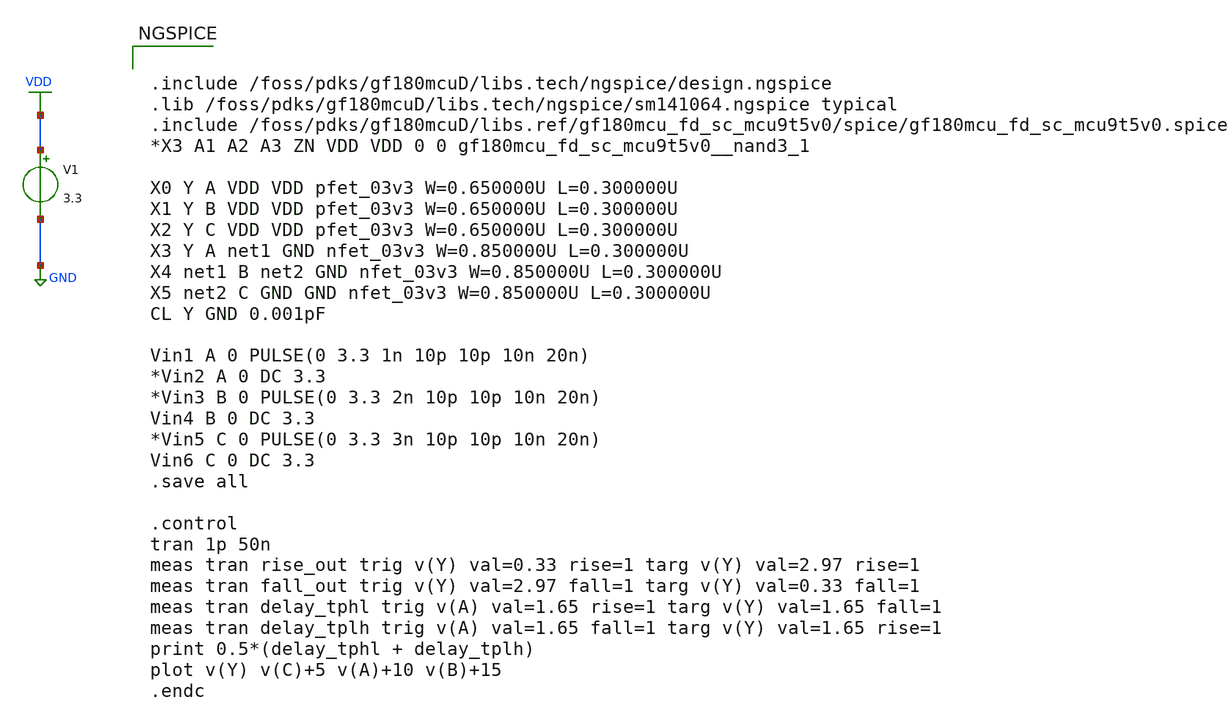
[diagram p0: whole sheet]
** sch_path: designs/libs/tb_NAND3/nand3_test.sch
**.subckt nand3_test
V1 VDD GND 3.3
**** begin user architecture code


.include /foss/pdks/gf180mcuD/libs.tech/ngspice/design.ngspice
.lib /foss/pdks/gf180mcuD/libs.tech/ngspice/sm141064.ngspice typical
.include /foss/pdks/gf180mcuD/libs.ref/gf180mcu_fd_sc_mcu9t5v0/spice/gf180mcu_fd_sc_mcu9t5v0.spice
*X3 A1 A2 A3 ZN VDD VDD 0 0 gf180mcu_fd_sc_mcu9t5v0__nand3_1

X0 Y A VDD VDD pfet_03v3 W=0.650000U L=0.300000U
X1 Y B VDD VDD pfet_03v3 W=0.650000U L=0.300000U
X2 Y C VDD VDD pfet_03v3 W=0.650000U L=0.300000U
X3 Y A net1 GND nfet_03v3 W=0.850000U L=0.300000U
X4 net1 B net2 GND nfet_03v3 W=0.850000U L=0.300000U
X5 net2 C GND GND nfet_03v3 W=0.850000U L=0.300000U
CL Y GND 0.001pF

Vin1 A 0 PULSE(0 3.3 1n 10p 10p 10n 20n)
*Vin2 A 0 DC 3.3
*Vin3 B 0 PULSE(0 3.3 2n 10p 10p 10n 20n)
Vin4 B 0 DC 3.3
*Vin5 C 0 PULSE(0 3.3 3n 10p 10p 10n 20n)
Vin6 C 0 DC 3.3
.save all

.control
tran 1p 50n
meas tran rise_out trig v(Y) val=0.33 rise=1 targ v(Y) val=2.97 rise=1
meas tran fall_out trig v(Y) val=2.97 fall=1 targ v(Y) val=0.33 fall=1
meas tran delay_tphl trig v(A) val=1.65 rise=1 targ v(Y) val=1.65 fall=1
meas tran delay_tplh trig v(A) val=1.65 fall=1 targ v(Y) val=1.65 rise=1
print 0.5*(delay_tphl + delay_tplh)
plot v(Y) v(C)+5 v(A)+10 v(B)+15
.endc


**** end user architecture code
**.ends
.GLOBAL VDD
.GLOBAL GND
.end
